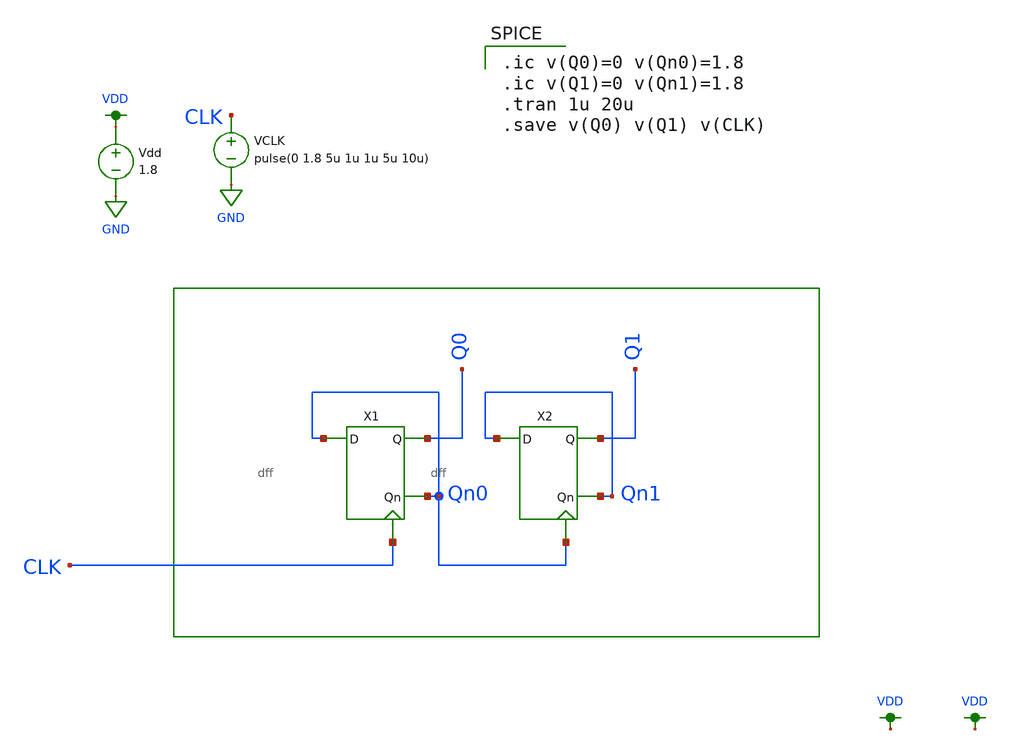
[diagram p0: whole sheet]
** sch_path: schematic/counter_new.sch
**.subckt counter_new
Vdd VDD GND 1.8
VCLK CLK GND pulse(0 1.8 5u 1u 1u 5u 10u)
X1 Qn0 Qn0 Q0 CLK dff
X2 Qn1 Qn1 Q1 Qn0 dff
**** begin user architecture code

.ic v(Q0)=0 v(Qn0)=1.8
.ic v(Q1)=0 v(Qn1)=1.8
.tran 1u 20u
.save v(Q0) v(Q1) v(CLK)


.option wnflag=1
.param MC_SWITCH=0.0
.lib ~/skywater/skywater-pdk/libraries/sky130_fd_pr_ngspice/latest/models/sky130.lib.spice tt

**** end user architecture code
**.ends

* expanding   symbol:  /home/madvlsi/Documents/MADVLSI-Final_Project/schematic/dff.sym # of pins=4
** sym_path: schematic/dff.sym
** sch_path: schematic/dff.sch
.subckt dff D Qn Q CLK
*.ipin D
*.iopin CLK
*.opin Qn
*.opin Q
X2 D CLK net1 VDD GND nand2
X3 net3 CLK net2 VDD GND nand2
X4 Q net2 Qn VDD GND nand2
X5 net1 Qn Q VDD GND nand2
X1 D net3 VDD GND inverter
.ends


* expanding   symbol:  /home/madvlsi/Documents/MADVLSI-Final_Project/schematic/nand2.sym # of pins=5
** sym_path: schematic/nand2.sym
** sch_path: schematic/nand2.sch
.subckt nand2 A B Y VP VN
*.ipin A
*.opin Y
*.ipin B
*.iopin VP
*.iopin VP
*.iopin VN
*.iopin VN
XM1 Y A VP VP sky130_fd_pr__pfet_01v8 L=0.15 W=2 nf=1 ad='int((nf+1)/2) * W/nf * 0.29' as='int((nf+2)/2) * W/nf * 0.29'
+ pd='2*int((nf+1)/2) * (W/nf + 0.29)' ps='2*int((nf+2)/2) * (W/nf + 0.29)' nrd='0.29 / W' nrs='0.29 / W'
+ sa=0 sb=0 sd=0 mult=1 m=1
XM2 VP B Y VP sky130_fd_pr__pfet_01v8 L=0.15 W=2 nf=1 ad='int((nf+1)/2) * W/nf * 0.29' as='int((nf+2)/2) * W/nf * 0.29'
+ pd='2*int((nf+1)/2) * (W/nf + 0.29)' ps='2*int((nf+2)/2) * (W/nf + 0.29)' nrd='0.29 / W' nrs='0.29 / W'
+ sa=0 sb=0 sd=0 mult=1 m=1
XM3 net1 B Y VN sky130_fd_pr__nfet_01v8 L=0.15 W=2 nf=1 ad='int((nf+1)/2) * W/nf * 0.29' as='int((nf+2)/2) * W/nf * 0.29'
+ pd='2*int((nf+1)/2) * (W/nf + 0.29)' ps='2*int((nf+2)/2) * (W/nf + 0.29)' nrd='0.29 / W' nrs='0.29 / W'
+ sa=0 sb=0 sd=0 mult=1 m=1
XM4 net1 A VN VN sky130_fd_pr__nfet_01v8 L=0.15 W=2 nf=1 ad='int((nf+1)/2) * W/nf * 0.29' as='int((nf+2)/2) * W/nf * 0.29'
+ pd='2*int((nf+1)/2) * (W/nf + 0.29)' ps='2*int((nf+2)/2) * (W/nf + 0.29)' nrd='0.29 / W' nrs='0.29 / W'
+ sa=0 sb=0 sd=0 mult=1 m=1
.ends


* expanding   symbol:  /home/madvlsi/Documents/MADVLSI-Final_Project/schematic/inverter.sym # of
*+ pins=4
** sym_path: schematic/inverter.sym
** sch_path: schematic/inverter.sch
.subckt inverter A Y VP VN
*.opin Y
*.ipin A
*.iopin VP
*.iopin VN
XM3 Y A VP VDD sky130_fd_pr__pfet_01v8 L={Lp} W={Wp} nf=1 ad='int((nf+1)/2) * W/nf * 0.29' as='int((nf+2)/2) * W/nf * 0.29'
+ pd='2*int((nf+1)/2) * (W/nf + 0.29)' ps='2*int((nf+2)/2) * (W/nf + 0.29)' nrd='0.29 / W' nrs='0.29 / W'
+ sa=0 sb=0 sd=0 mult=1 m=1
XM4 Y A VP VDD sky130_fd_pr__pfet_01v8 L={Lp} W={Wp} nf=1 ad='int((nf+1)/2) * W/nf * 0.29' as='int((nf+2)/2) * W/nf * 0.29'
+ pd='2*int((nf+1)/2) * (W/nf + 0.29)' ps='2*int((nf+2)/2) * (W/nf + 0.29)' nrd='0.29 / W' nrs='0.29 / W'
+ sa=0 sb=0 sd=0 mult=1 m=1
XM5 Y A VN GND sky130_fd_pr__nfet_01v8 L={Lp} W={Wp} nf=1 ad='int((nf+1)/2) * W/nf * 0.29' as='int((nf+2)/2) * W/nf * 0.29'
+ pd='2*int((nf+1)/2) * (W/nf + 0.29)' ps='2*int((nf+2)/2) * (W/nf + 0.29)' nrd='0.29 / W' nrs='0.29 / W'
+ sa=0 sb=0 sd=0 mult=1 m=1
.ends

.GLOBAL GND
.GLOBAL VDD
.end
